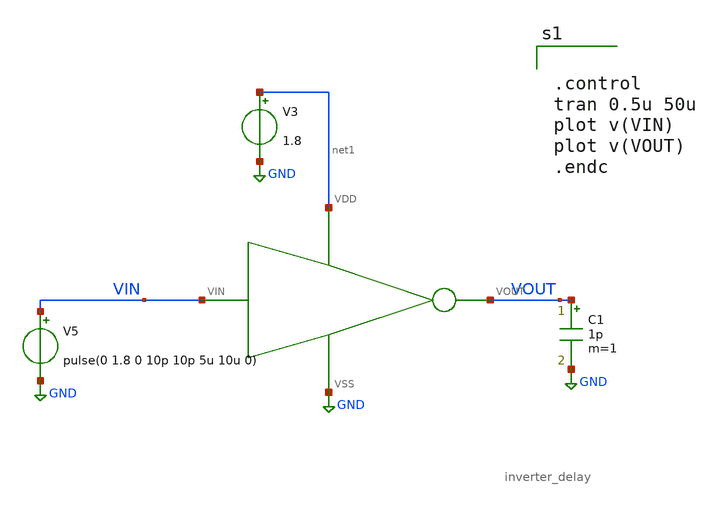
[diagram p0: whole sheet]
** sch_path: xschem/DC_DC_Converter_xschem/OTHERS/DC_DC_Converter_JV11/Delay_block_revised/Inverter_TB.sch
**.subckt Inverter_TB
V3 net1 GND 1.8
V5 VIN GND pulse(0 1.8 0 10p 10p 5u 10u 0)
C1 VOUT GND 1p m=1
X2 VOUT VIN net1 GND inverter_delay
**** begin user architecture code

** opencircuitdesign pdks install
.lib $::SKYWATER_MODELS/sky130.lib.spice tt




.control
tran 0.5u 50u
plot v(VIN)
plot v(VOUT)
.endc


**** end user architecture code
**.ends

* expanding   symbol:  DC_DC_Converter/Delay_block_revised/inverter_delay.sym # of pins=4
** sym_path: xschem/DC_DC_Converter_xschem/DC_DC_Converter/Delay_block_revised/inverter_delay.sym
** sch_path: xschem/DC_DC_Converter_xschem/DC_DC_Converter/Delay_block_revised/inverter_delay.sch
.subckt inverter_delay VOUT VIN VDD VSS
*.iopin VDD
*.iopin VOUT
*.iopin VSS
*.iopin VIN
XM1 VOUT VIN VSS VSS sky130_fd_pr__nfet_01v8 L=0.15 W=0.4 nf=1 ad='int((nf+1)/2) * W/nf * 0.29' as='int((nf+2)/2) * W/nf * 0.29'
+ pd='2*int((nf+1)/2) * (W/nf + 0.29)' ps='2*int((nf+2)/2) * (W/nf + 0.29)' nrd='0.29 / W' nrs='0.29 / W'
+ sa=0 sb=0 sd=0 mult=1 m=1
XM2 VOUT VIN VDD VDD sky130_fd_pr__pfet_01v8 L=0.15 W=0.6 nf=1 ad='int((nf+1)/2) * W/nf * 0.29' as='int((nf+2)/2) * W/nf * 0.29'
+ pd='2*int((nf+1)/2) * (W/nf + 0.29)' ps='2*int((nf+2)/2) * (W/nf + 0.29)' nrd='0.29 / W' nrs='0.29 / W'
+ sa=0 sb=0 sd=0 mult=2 m=2
.ends

.GLOBAL GND
.end
